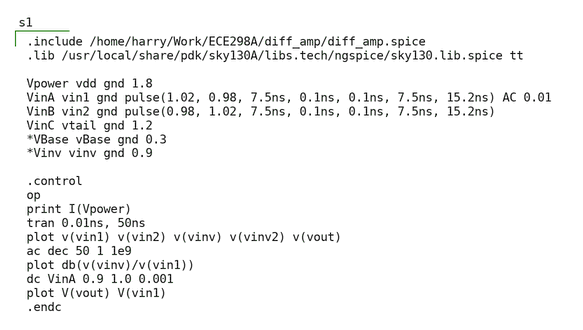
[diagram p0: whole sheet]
** sch_path: magic_xschem_ngspice/Magic_sim.sch
**.subckt Magic_sim
**** begin user architecture code

.include /home/harry/Work/ECE298A/diff_amp/diff_amp.spice
.lib /usr/local/share/pdk/sky130A/libs.tech/ngspice/sky130.lib.spice tt

Vpower vdd gnd 1.8
VinA vin1 gnd pulse(1.02, 0.98, 7.5ns, 0.1ns, 0.1ns, 7.5ns, 15.2ns) AC 0.01
VinB vin2 gnd pulse(0.98, 1.02, 7.5ns, 0.1ns, 0.1ns, 7.5ns, 15.2ns)
VinC vtail gnd 1.2
*VBase vBase gnd 0.3
*Vinv vinv gnd 0.9

.control
op
print I(Vpower)
tran 0.01ns, 50ns
plot v(vin1) v(vin2) v(vinv) v(vinv2) v(vout)
ac dec 50 1 1e9
plot db(v(vinv)/v(vin1))
dc VinA 0.9 1.0 0.001
plot V(vout) V(vin1)
.endc

**** end user architecture code
**.ends
.end
